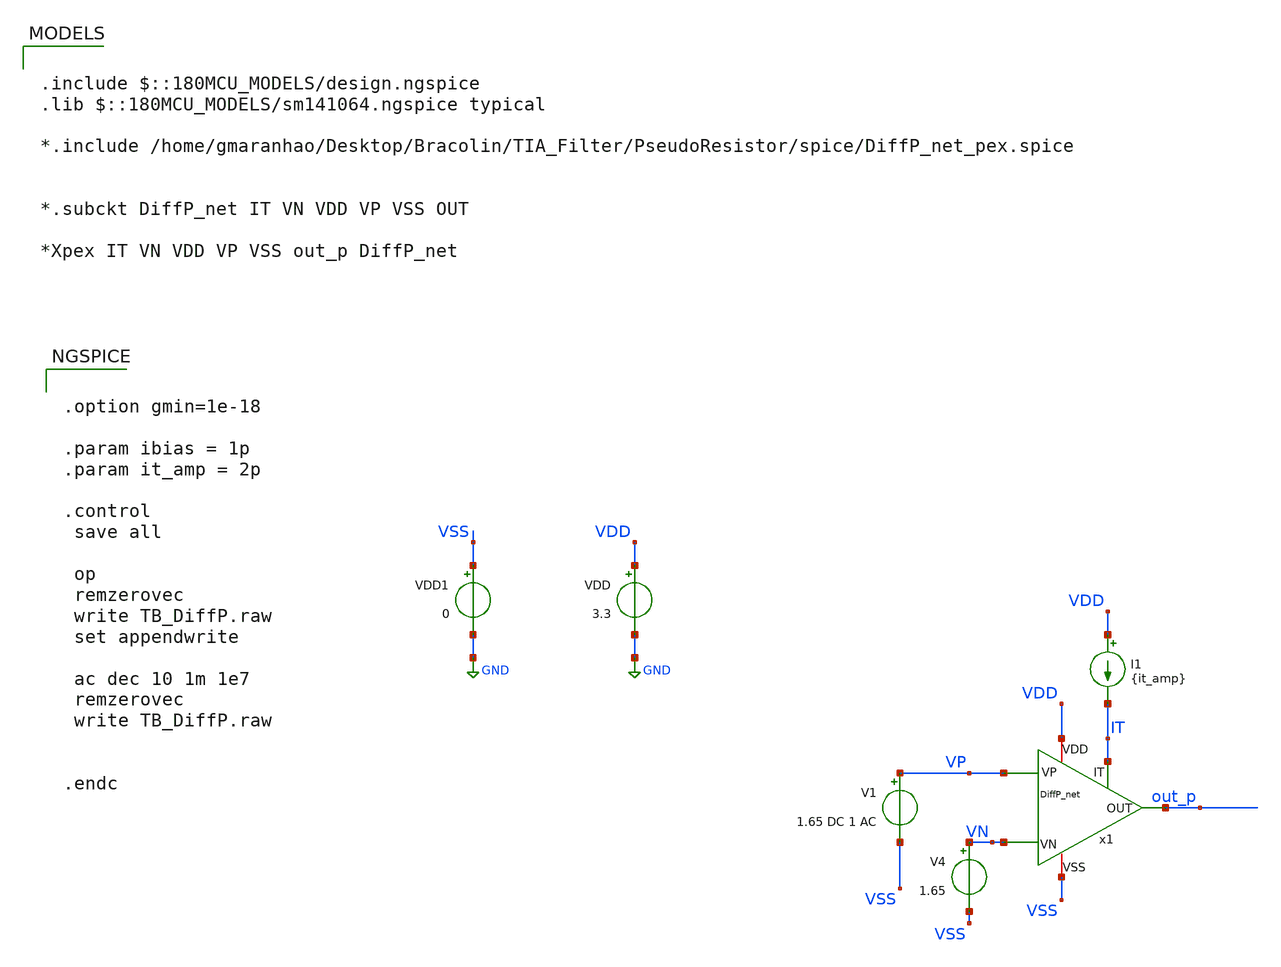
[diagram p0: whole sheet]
** sch_path: TIA_Filter/PseudoResistor/TB_DiffP.sch
**.subckt TB_DiffP
V1 VP VSS 1.65 DC 1 AC
V4 VN VSS 1.65
I1 VDD IT {it_amp}
x1 VN VP out_p IT VDD VSS DiffP_net
VDD VDD GND 3.3
VDD1 VSS GND 0
**** begin user architecture code

.include $::180MCU_MODELS/design.ngspice
.lib $::180MCU_MODELS/sm141064.ngspice typical

*.include /home/gmaranhao/Desktop/Bracolin/TIA_Filter/PseudoResistor/spice/DiffP_net_pex.spice


*.subckt DiffP_net IT VN VDD VP VSS OUT

*Xpex IT VN VDD VP VSS out_p DiffP_net




.option gmin=1e-18

.param ibias = 1p
.param it_amp = 2p

.control
 save all

 op
 remzerovec
 write TB_DiffP.raw
 set appendwrite

 ac dec 10 1m 1e7
 remzerovec
 write TB_DiffP.raw


.endc


**** end user architecture code
**.ends
.GLOBAL GND
.end
